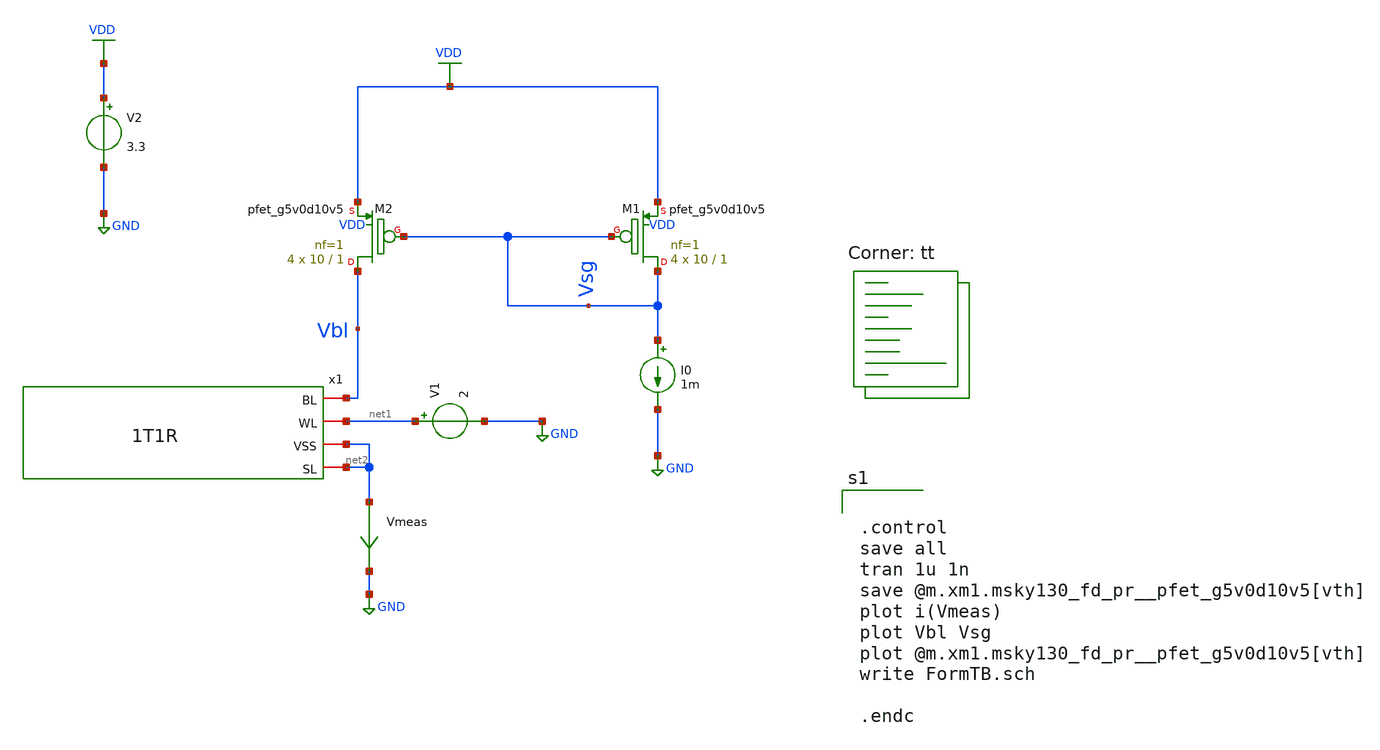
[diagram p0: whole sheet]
** sch_path: xschem/Crossbar/FormTB.sch
* StefanSchippers/xschem_sky130/sky130_fd_pr/reram.sym:
* Copyright 2021 Stefan Frederik Schippers
* Licensed under the Apache License, Version 2.0 (the "License");
**.subckt FormTB
x1 Vbl net1 net2 net2 1T1R
I0 Vsg GND 1m
V1 net1 GND 2
V2 VDD GND 3.3
XM1 Vsg Vsg VDD VDD sky130_fd_pr__pfet_g5v0d10v5 L=1 W=10 nf=1 ad='int((nf+1)/2) * W/nf * 0.29' as='int((nf+2)/2) * W/nf * 0.29'
+ pd='2*int((nf+1)/2) * (W/nf + 0.29)' ps='2*int((nf+2)/2) * (W/nf + 0.29)' nrd='0.29 / W' nrs='0.29 / W'
+ sa=0 sb=0 sd=0 mult=4 m=4
XM2 Vbl Vsg VDD VDD sky130_fd_pr__pfet_g5v0d10v5 L=1 W=10 nf=1 ad='int((nf+1)/2) * W/nf * 0.29' as='int((nf+2)/2) * W/nf * 0.29'
+ pd='2*int((nf+1)/2) * (W/nf + 0.29)' ps='2*int((nf+2)/2) * (W/nf + 0.29)' nrd='0.29 / W' nrs='0.29 / W'
+ sa=0 sb=0 sd=0 mult=4 m=4
Vmeas net2 GND 0
.save i(vmeas)
**** begin user architecture code
.lib $::SKYWATER_MODELS/sky130.lib.spice tt


.control
save all
tran 1u 1n
save @m.xm1.msky130_fd_pr__pfet_g5v0d10v5[vth]
plot i(Vmeas)
plot Vbl Vsg
plot @m.xm1.msky130_fd_pr__pfet_g5v0d10v5[vth]
write FormTB.sch

.endc


**** end user architecture code
**.ends

* expanding   symbol:  Crossbar/1T1R.sym # of pins=4
** sym_path: xschem/1T1R.sym
** sch_path: xschem/1T1R.sch
.subckt 1T1R BL WL VSS SL
*.iopin SL
*.iopin VSS
*.iopin WL
*.iopin BL
XR1 BL net1 sky130_fd_pr_reram__reram_cell Tfilament_0=3.8e-9
XM1 net1 WL SL VSS sky130_fd_pr__nfet_g5v0d10v5 L=0.5 W=7 nf=1 ad='int((nf+1)/2) * W/nf * 0.29' as='int((nf+2)/2) * W/nf * 0.29'
+ pd='2*int((nf+1)/2) * (W/nf + 0.29)' ps='2*int((nf+2)/2) * (W/nf + 0.29)' nrd='0.29 / W' nrs='0.29 / W'
+ sa=0 sb=0 sd=0 mult=1 m=1
.ends

.GLOBAL GND
.GLOBAL VDD
**** begin user architecture code

.subckt sky130_fd_pr_reram__reram_cell TE BE Tfilament_0=3.3e-9 area_ox=0.1024e-12
N1 TE BE nFilament sky130_fd_pr_reram__reram_model
.ic v(nFilament)={Tfilament_0*1.0e9}
.ends sky130_fd_pr_reram__reram_cell

.model sky130_fd_pr_reram__reram_model sky130_fd_pr_reram__reram_module  area_ox = 0.1024e-12  Tox =
+ 5.0  Tfilament_max = 4.9  Tfilament_min = 3.3  Eact_generation = 1.501  Eact_recombination  = 1.500
+  I_k1  = 6.140e-5  Tfilament_ref = 4.7249  V_ref = 0.430  velocity_k1 = 150  gamma_k0  = 16.5  gamma_k1
+  = -1.25  Temperature_0 = 300  C_thermal = 3.1825e-16  tau_thermal = 0.23e-9  t_step  = 1.0e-9
+  smoothing = 1e-7  Kclip = 200

.control
pre_osdi $SKYWATER_MODELS/sky130_fd_pr_reram__reram_module.osdi
.endc

**** end user architecture code
.end
